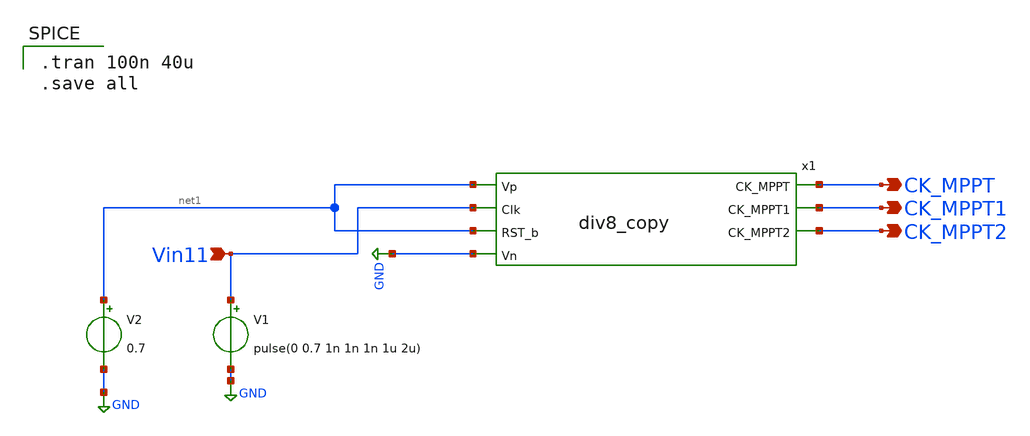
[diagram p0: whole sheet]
** sch_path: Blocks/MPPT/DIV8_test.sch
**.subckt DIV8_test CK_MPPT CK_MPPT1 CK_MPPT2 Vin11
*.opin CK_MPPT
*.opin CK_MPPT1
*.opin CK_MPPT2
*.ipin Vin11
x1 net1 Vin11 CK_MPPT net1 GND CK_MPPT1 CK_MPPT2 div8_copy
V1 Vin11 GND pulse(0 0.7 1n 1n 1n 1u 2u)
V2 net1 GND 0.7
**** begin user architecture code

** opencircuitdesign pdks install
.lib $::SKYWATER_MODELS/sky130.lib.spice tt



.tran 100n 40u
.save all

**** end user architecture code
**.ends

* expanding   symbol:  PICO_2022/div8_copy.sym # of pins=7
** sym_path: Blocks/MPPT/div8_copy.sym
** sch_path: Blocks/MPPT/div8_copy.sch
.subckt div8_copy Vp Clk CK_MPPT RST_b Vn CK_MPPT1 CK_MPPT2
*.ipin Clk
*.ipin RST_b
*.opin CK_MPPT
*.opin CK_MPPT1
*.opin CK_MPPT2
*.ipin Vn
*.ipin Vp
x1 net2 Clk RST_b Vn Vp net1 net2 DFF1
x2 net3 net1 RST_b Vn Vp net4 net3 DFF1
x3 net6 net4 RST_b Vn Vp net5 net6 DFF1
x4 net7 CK_MPPT Vp Vn INV
x5 net8 CK_MPPT1 Vp Vn INV
x7 net9 CK_MPPT2 Vp Vn INV
x8 net1 net12 Vp Vn INV
x11 net4 net11 Vp Vn INV
x12 net4 net10 Vp Vn INV
x6 net5 net11 net12 Vp Vn net9 NAND3
x9 net5 net10 net1 Vp Vn net8 NAND3
x10 net5 net4 net1 Vp Vn net7 NAND3
.ends


* expanding   symbol:  component/FlipFlops/DFF1.sym # of pins=7
** sym_path: component/FlipFlops/DFF1.sym
** sch_path: component/FlipFlops/DFF1.sch
.subckt DFF1 D Clk RST VN VP Q Qb
*.opin Q
*.iopin VN
*.iopin VP
*.ipin Clk
*.ipin D
*.ipin RST
*.opin Qb
x7 net2 net4 net3 VP VN NAND
x8 net3 Clk RST VP VN net2 NAND3
x6 Q net1 RST VP VN Qb NAND3
x4 net2 Clk net4 VP VN net1 NAND3
x5 net1 D RST VP VN net4 NAND3
x1 Qb net2 Q VP VN NAND
.ends


* expanding   symbol:  component/INV/INV.sym # of pins=4
** sym_path: component/INV/INV.sym
** sch_path: component/INV/INV.sch
.subckt INV X Y VP VN
*.ipin X
*.opin Y
*.iopin VN
*.iopin VP
XM1 Y X VN VN sky130_fd_pr__nfet_01v8 L=0.15 W=0.42 nf=1 ad='int((nf+1)/2) * W/nf * 0.29' as='int((nf+2)/2) * W/nf * 0.29'
+ pd='2*int((nf+1)/2) * (W/nf + 0.29)' ps='2*int((nf+2)/2) * (W/nf + 0.29)' nrd='0.29 / W' nrs='0.29 / W'
+ sa=0 sb=0 sd=0 mult=1 m=1
XM2 Y X VP VP sky130_fd_pr__pfet_01v8 L=0.15 W=1.26 nf=1 ad='int((nf+1)/2) * W/nf * 0.29' as='int((nf+2)/2) * W/nf * 0.29'
+ pd='2*int((nf+1)/2) * (W/nf + 0.29)' ps='2*int((nf+2)/2) * (W/nf + 0.29)' nrd='0.29 / W' nrs='0.29 / W'
+ sa=0 sb=0 sd=0 mult=1 m=1
.ends


* expanding   symbol:  component/NAND3/NAND3.sym # of pins=6
** sym_path: component/NAND3/NAND3.sym
** sch_path: component/NAND3/NAND3.sch
.subckt NAND3 A B C VP VN Y
*.iopin VP
*.iopin VN
*.ipin A
*.ipin B
*.ipin C
*.opin Y
XM1 Y A net1 VN sky130_fd_pr__nfet_01v8 L=0.15 W=1.26 nf=1 ad='int((nf+1)/2) * W/nf * 0.29' as='int((nf+2)/2) * W/nf * 0.29'
+ pd='2*int((nf+1)/2) * (W/nf + 0.29)' ps='2*int((nf+2)/2) * (W/nf + 0.29)' nrd='0.29 / W' nrs='0.29 / W'
+ sa=0 sb=0 sd=0 mult=1 m=1
XM2 net1 B net2 VN sky130_fd_pr__nfet_01v8 L=0.15 W=1.26 nf=1 ad='int((nf+1)/2) * W/nf * 0.29' as='int((nf+2)/2) * W/nf * 0.29'
+ pd='2*int((nf+1)/2) * (W/nf + 0.29)' ps='2*int((nf+2)/2) * (W/nf + 0.29)' nrd='0.29 / W' nrs='0.29 / W'
+ sa=0 sb=0 sd=0 mult=1 m=1
XM3 net2 C VN VN sky130_fd_pr__nfet_01v8 L=0.15 W=1.26 nf=1 ad='int((nf+1)/2) * W/nf * 0.29' as='int((nf+2)/2) * W/nf * 0.29'
+ pd='2*int((nf+1)/2) * (W/nf + 0.29)' ps='2*int((nf+2)/2) * (W/nf + 0.29)' nrd='0.29 / W' nrs='0.29 / W'
+ sa=0 sb=0 sd=0 mult=1 m=1
XM4 Y A VP VP sky130_fd_pr__pfet_01v8 L=0.15 W=1.26 nf=1 ad='int((nf+1)/2) * W/nf * 0.29' as='int((nf+2)/2) * W/nf * 0.29'
+ pd='2*int((nf+1)/2) * (W/nf + 0.29)' ps='2*int((nf+2)/2) * (W/nf + 0.29)' nrd='0.29 / W' nrs='0.29 / W'
+ sa=0 sb=0 sd=0 mult=1 m=1
XM5 Y B VP VP sky130_fd_pr__pfet_01v8 L=0.15 W=1.26 nf=1 ad='int((nf+1)/2) * W/nf * 0.29' as='int((nf+2)/2) * W/nf * 0.29'
+ pd='2*int((nf+1)/2) * (W/nf + 0.29)' ps='2*int((nf+2)/2) * (W/nf + 0.29)' nrd='0.29 / W' nrs='0.29 / W'
+ sa=0 sb=0 sd=0 mult=1 m=1
XM6 Y C VP VP sky130_fd_pr__pfet_01v8 L=0.15 W=1.26 nf=1 ad='int((nf+1)/2) * W/nf * 0.29' as='int((nf+2)/2) * W/nf * 0.29'
+ pd='2*int((nf+1)/2) * (W/nf + 0.29)' ps='2*int((nf+2)/2) * (W/nf + 0.29)' nrd='0.29 / W' nrs='0.29 / W'
+ sa=0 sb=0 sd=0 mult=1 m=1
.ends


* expanding   symbol:  component/NAND2/NAND.sym # of pins=5
** sym_path: component/NAND2/NAND.sym
** sch_path: component/NAND2/NAND.sch
.subckt NAND B A Y VP VN
*.iopin VP
*.ipin A
*.ipin B
*.opin Y
*.iopin VN
XM1 Y A VP VP sky130_fd_pr__pfet_01v8 L=0.15 W=1.26 nf=1 ad='int((nf+1)/2) * W/nf * 0.29' as='int((nf+2)/2) * W/nf * 0.29'
+ pd='2*int((nf+1)/2) * (W/nf + 0.29)' ps='2*int((nf+2)/2) * (W/nf + 0.29)' nrd='0.29 / W' nrs='0.29 / W'
+ sa=0 sb=0 sd=0 mult=1 m=1
XM2 Y B VP VP sky130_fd_pr__pfet_01v8 L=0.15 W=1.26 nf=1 ad='int((nf+1)/2) * W/nf * 0.29' as='int((nf+2)/2) * W/nf * 0.29'
+ pd='2*int((nf+1)/2) * (W/nf + 0.29)' ps='2*int((nf+2)/2) * (W/nf + 0.29)' nrd='0.29 / W' nrs='0.29 / W'
+ sa=0 sb=0 sd=0 mult=1 m=1
XM3 Y A net1 net1 sky130_fd_pr__nfet_01v8 L=0.15 W=0.84 nf=1 ad='int((nf+1)/2) * W/nf * 0.29' as='int((nf+2)/2) * W/nf * 0.29'
+ pd='2*int((nf+1)/2) * (W/nf + 0.29)' ps='2*int((nf+2)/2) * (W/nf + 0.29)' nrd='0.29 / W' nrs='0.29 / W'
+ sa=0 sb=0 sd=0 mult=1 m=1
XM4 net1 B VN VN sky130_fd_pr__nfet_01v8 L=0.15 W=0.84 nf=1 ad='int((nf+1)/2) * W/nf * 0.29' as='int((nf+2)/2) * W/nf * 0.29'
+ pd='2*int((nf+1)/2) * (W/nf + 0.29)' ps='2*int((nf+2)/2) * (W/nf + 0.29)' nrd='0.29 / W' nrs='0.29 / W'
+ sa=0 sb=0 sd=0 mult=1 m=1
.ends

.GLOBAL GND
.end
